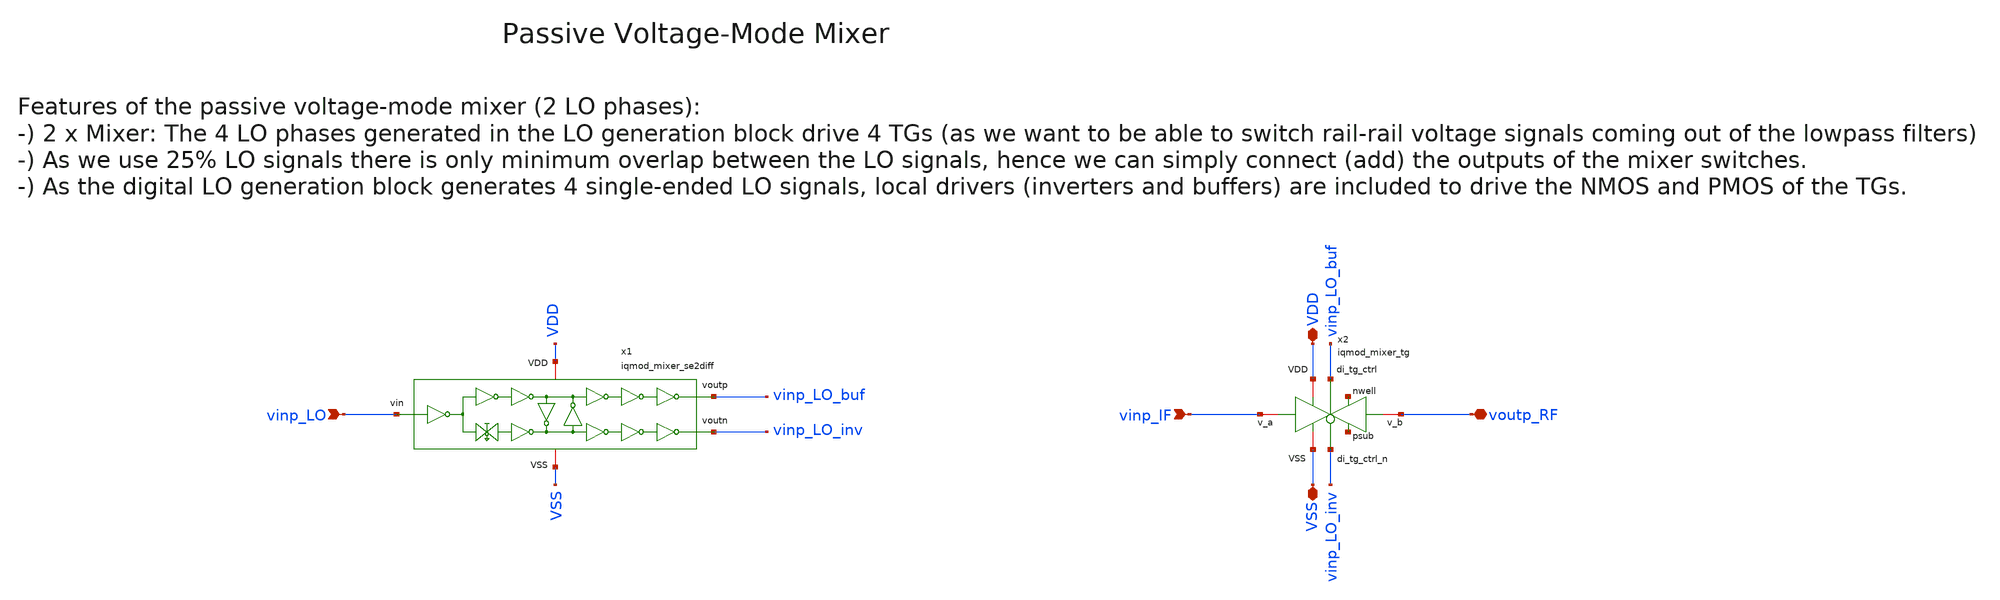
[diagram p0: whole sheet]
** sch_path: ihp130/macros/iqmod/schematic/iqmod_mixer_half.sch
**.subckt iqmod_mixer_half VDD VSS vinp_IF voutp_RF vinp_LO
*.iopin VDD
*.iopin VSS
*.ipin vinp_IF
*.iopin voutp_RF
*.ipin vinp_LO
x2 net1 net2 VDD vinp_LO_buf VSS voutp_RF vinp_IF vinp_LO_inv iqmod_mixer_tg
x1 VDD vinp_LO vinp_LO_buf VSS vinp_LO_inv iqmod_mixer_se2diff
**.ends
.end
